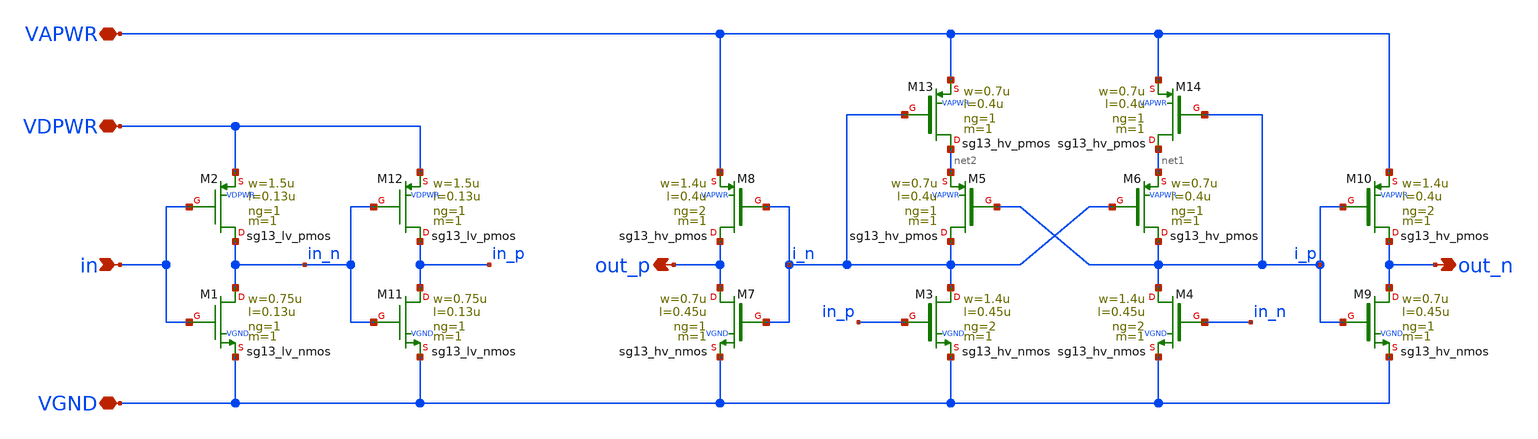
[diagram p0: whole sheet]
** sch_path: pg/ihp-sg13cmos5l/tt_pg_3v3_2/xschem/lv2hv.sch
**.subckt lv2hv VAPWR VGND in VDPWR out_p out_n
*.iopin VAPWR
*.iopin VGND
*.ipin in
*.iopin VDPWR
*.opin out_p
*.opin out_n
XM1 in_n in VGND VGND sg13_lv_nmos w=0.75u l=0.13u ng=1 m=1
XM2 in_n in VDPWR VDPWR sg13_lv_pmos w=1.5u l=0.13u ng=1 m=1
XM11 in_p in_n VGND VGND sg13_lv_nmos w=0.75u l=0.13u ng=1 m=1
XM12 in_p in_n VDPWR VDPWR sg13_lv_pmos w=1.5u l=0.13u ng=1 m=1
XM3 i_n in_p VGND VGND sg13_hv_nmos w=1.4u l=0.45u ng=2 m=1
XM4 i_p in_n VGND VGND sg13_hv_nmos w=1.4u l=0.45u ng=2 m=1
XM5 i_n i_p net2 VAPWR sg13_hv_pmos w=0.7u l=0.4u ng=1 m=1
XM6 i_p i_n net1 VAPWR sg13_hv_pmos w=0.7u l=0.4u ng=1 m=1
XM7 out_p i_n VGND VGND sg13_hv_nmos w=0.7u l=0.45u ng=1 m=1
XM8 out_p i_n VAPWR VAPWR sg13_hv_pmos w=1.4u l=0.4u ng=2 m=1
XM9 out_n i_p VGND VGND sg13_hv_nmos w=0.7u l=0.45u ng=1 m=1
XM10 out_n i_p VAPWR VAPWR sg13_hv_pmos w=1.4u l=0.4u ng=2 m=1
XM13 net2 i_n VAPWR VAPWR sg13_hv_pmos w=0.7u l=0.4u ng=1 m=1
XM14 net1 i_p VAPWR VAPWR sg13_hv_pmos w=0.7u l=0.4u ng=1 m=1
**.ends
.end
